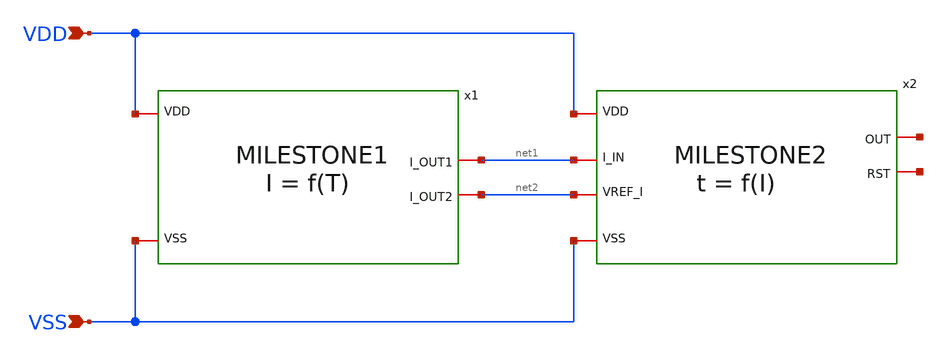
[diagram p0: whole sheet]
** sch_path: design/CNR_GR03_SKY130NM/TOPLEVEL.sch
**.subckt TOPLEVEL VDD VSS
*.ipin VDD
*.ipin VSS
x1 VDD net1 net2 VSS MILESTONE1
x2 net1 net2 net3 VDD net4 VSS MILESTONE2
**.ends
.end
